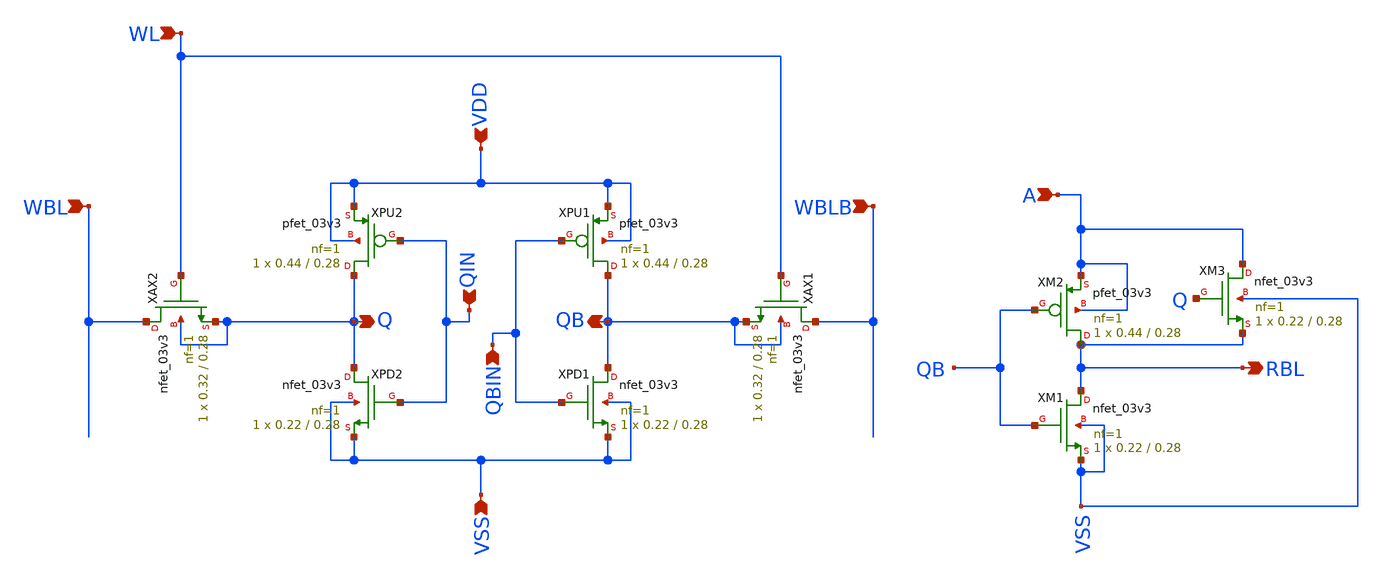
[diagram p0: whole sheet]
** sch_path: analog/designs/9T_03v3.sch
**.subckt 9T_03v3 RBL VSS VDD WL WBL WBLB QBIN QIN Q QB A
*.opin RBL
*.ipin VSS
*.ipin VDD
*.ipin WL
*.ipin WBL
*.ipin WBLB
*.ipin QBIN
*.ipin QIN
*.opin Q
*.opin QB
*.ipin A
XM1 RBL QB VSS VSS nfet_03v3 L=0.28 W=0.22 nf=1 ad='int((nf+1)/2) * W/nf * 0.18u' as='int((nf+2)/2) * W/nf * 0.18u'
+ pd='2*int((nf+1)/2) * (W/nf + 0.18u)' ps='2*int((nf+2)/2) * (W/nf + 0.18u)' nrd='0.18u / W' nrs='0.18u / W'
+ sa=0 sb=0 sd=0 m=1
XPD1 QB QBIN VSS VSS nfet_03v3 L=0.28 W=0.22 nf=1 ad='int((nf+1)/2) * W/nf * 0.18u' as='int((nf+2)/2) * W/nf * 0.18u'
+ pd='2*int((nf+1)/2) * (W/nf + 0.18u)' ps='2*int((nf+2)/2) * (W/nf + 0.18u)' nrd='0.18u / W' nrs='0.18u / W'
+ sa=0 sb=0 sd=0 m=1
XPU1 QB QBIN VDD VDD pfet_03v3 L=0.28 W=0.44 nf=1 ad='int((nf+1)/2) * W/nf * 0.18u' as='int((nf+2)/2) * W/nf * 0.18u'
+ pd='2*int((nf+1)/2) * (W/nf + 0.18u)' ps='2*int((nf+2)/2) * (W/nf + 0.18u)' nrd='0.18u / W' nrs='0.18u / W'
+ sa=0 sb=0 sd=0 m=1
XAX1 WBLB WL QB QB nfet_03v3 L=0.28 W=0.32 nf=1 ad='int((nf+1)/2) * W/nf * 0.18u' as='int((nf+2)/2) * W/nf * 0.18u'
+ pd='2*int((nf+1)/2) * (W/nf + 0.18u)' ps='2*int((nf+2)/2) * (W/nf + 0.18u)' nrd='0.18u / W' nrs='0.18u / W'
+ sa=0 sb=0 sd=0 m=1
XPU2 Q QIN VDD VDD pfet_03v3 L=0.28 W=0.44 nf=1 ad='int((nf+1)/2) * W/nf * 0.18u' as='int((nf+2)/2) * W/nf * 0.18u'
+ pd='2*int((nf+1)/2) * (W/nf + 0.18u)' ps='2*int((nf+2)/2) * (W/nf + 0.18u)' nrd='0.18u / W' nrs='0.18u / W'
+ sa=0 sb=0 sd=0 m=1
XPD2 Q QIN VSS VSS nfet_03v3 L=0.28 W=0.22 nf=1 ad='int((nf+1)/2) * W/nf * 0.18u' as='int((nf+2)/2) * W/nf * 0.18u'
+ pd='2*int((nf+1)/2) * (W/nf + 0.18u)' ps='2*int((nf+2)/2) * (W/nf + 0.18u)' nrd='0.18u / W' nrs='0.18u / W'
+ sa=0 sb=0 sd=0 m=1
XAX2 WBL WL Q Q nfet_03v3 L=0.28 W=0.32 nf=1 ad='int((nf+1)/2) * W/nf * 0.18u' as='int((nf+2)/2) * W/nf * 0.18u'
+ pd='2*int((nf+1)/2) * (W/nf + 0.18u)' ps='2*int((nf+2)/2) * (W/nf + 0.18u)' nrd='0.18u / W' nrs='0.18u / W'
+ sa=0 sb=0 sd=0 m=1
XM2 RBL QB A A pfet_03v3 L=0.28 W=0.44 nf=1 ad='int((nf+1)/2) * W/nf * 0.18u' as='int((nf+2)/2) * W/nf * 0.18u'
+ pd='2*int((nf+1)/2) * (W/nf + 0.18u)' ps='2*int((nf+2)/2) * (W/nf + 0.18u)' nrd='0.18u / W' nrs='0.18u / W'
+ sa=0 sb=0 sd=0 m=1
XM3 A Q RBL VSS nfet_03v3 L=0.28 W=0.22 nf=1 ad='int((nf+1)/2) * W/nf * 0.18u' as='int((nf+2)/2) * W/nf * 0.18u'
+ pd='2*int((nf+1)/2) * (W/nf + 0.18u)' ps='2*int((nf+2)/2) * (W/nf + 0.18u)' nrd='0.18u / W' nrs='0.18u / W'
+ sa=0 sb=0 sd=0 m=1
**.ends
.end
